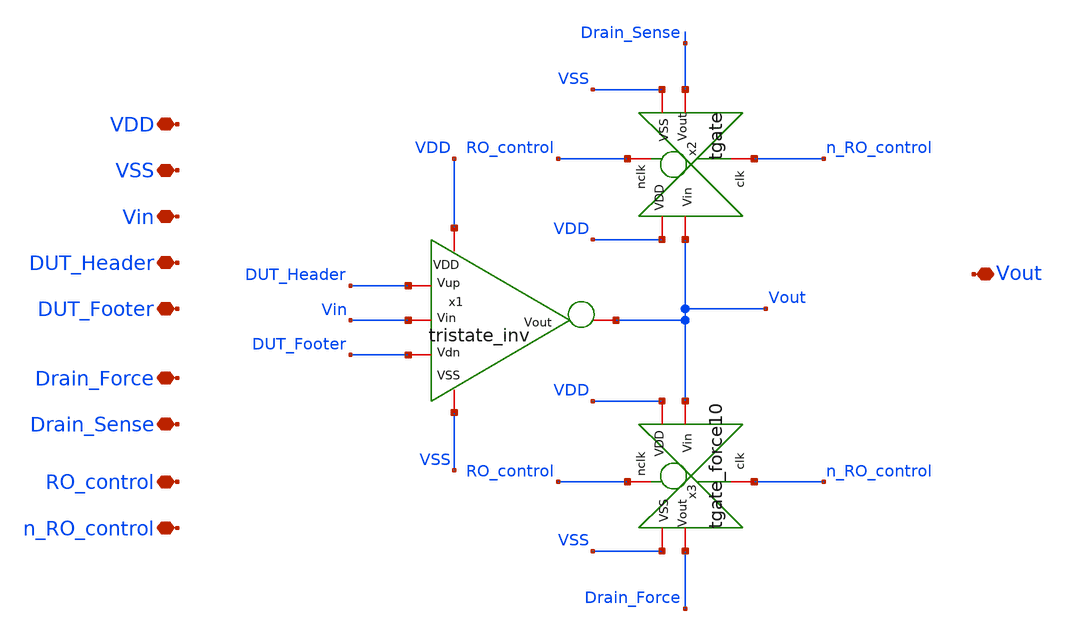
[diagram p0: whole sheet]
** sch_path: TT/rovcel1_10.sch
**.subckt rovcel1_10 VDD VSS Vin DUT_Header DUT_Footer Drain_Force Vout Drain_Sense RO_control
*+ n_RO_control
*.iopin VDD
*.iopin VSS
*.iopin Vin
*.iopin DUT_Header
*.iopin DUT_Footer
*.iopin Drain_Force
*.iopin Vout
*.iopin Drain_Sense
*.iopin RO_control
*.iopin n_RO_control
x1 VDD VSS Vin DUT_Header DUT_Footer Vout tristate_inv
x2 RO_control VDD Vout Drain_Sense VSS n_RO_control tgate
x3 RO_control VDD Vout Drain_Force VSS n_RO_control tgate_force10
**.ends

* expanding   symbol:  /foss/designs/Projects/RO_reliability/xschem/tristate_inv.sym # of pins=6
** sym_path: TT/tristate_inv.sym
** sch_path: TT/tristate_inv.sch
.subckt tristate_inv VDD VSS Vin Vup Vdn Vout
*.iopin VDD
*.iopin VSS
*.iopin Vin
*.iopin Vout
*.iopin Vup
*.iopin Vdn
XM1 net1 Vup VDD VDD sky130_fd_pr__pfet_01v8 L=0.15 W=4.75 nf=1 ad='int((nf+1)/2) * W/nf * 0.29' as='int((nf+2)/2) * W/nf * 0.29'
+ pd='2*int((nf+1)/2) * (W/nf + 0.29)' ps='2*int((nf+2)/2) * (W/nf + 0.29)' nrd='0.29 / W' nrs='0.29 / W'
+ sa=0 sb=0 sd=0 mult=40 m=40
XM2 Vout Vin net1 VDD sky130_fd_pr__pfet_01v8 L=0.15 W=4.75 nf=1 ad='int((nf+1)/2) * W/nf * 0.29' as='int((nf+2)/2) * W/nf * 0.29'
+ pd='2*int((nf+1)/2) * (W/nf + 0.29)' ps='2*int((nf+2)/2) * (W/nf + 0.29)' nrd='0.29 / W' nrs='0.29 / W'
+ sa=0 sb=0 sd=0 mult=4 m=4
XM3 Vout Vin net2 VSS sky130_fd_pr__nfet_01v8 L=0.15 W=2.1 nf=1 ad='int((nf+1)/2) * W/nf * 0.29' as='int((nf+2)/2) * W/nf * 0.29'
+ pd='2*int((nf+1)/2) * (W/nf + 0.29)' ps='2*int((nf+2)/2) * (W/nf + 0.29)' nrd='0.29 / W' nrs='0.29 / W'
+ sa=0 sb=0 sd=0 mult=2 m=2
XM4 net2 Vdn VSS VSS sky130_fd_pr__nfet_01v8 L=0.15 W=2.1 nf=1 ad='int((nf+1)/2) * W/nf * 0.29' as='int((nf+2)/2) * W/nf * 0.29'
+ pd='2*int((nf+1)/2) * (W/nf + 0.29)' ps='2*int((nf+2)/2) * (W/nf + 0.29)' nrd='0.29 / W' nrs='0.29 / W'
+ sa=0 sb=0 sd=0 mult=20 m=20
.ends


* expanding   symbol:  /foss/designs/Projects/RO_reliability/xschem/tgate.sym # of pins=6
** sym_path: TT/tgate.sym
** sch_path: TT/tgate.sch
.subckt tgate nclk VDD Vin Vout VSS clk
*.iopin nclk
*.iopin clk
*.iopin VDD
*.iopin VSS
*.iopin Vout
*.iopin Vin
XM1 Vin nclk Vout VDD sky130_fd_pr__pfet_01v8 L=0.15 W=0.45 nf=1 ad='int((nf+1)/2) * W/nf * 0.29' as='int((nf+2)/2) * W/nf * 0.29'
+ pd='2*int((nf+1)/2) * (W/nf + 0.29)' ps='2*int((nf+2)/2) * (W/nf + 0.29)' nrd='0.29 / W' nrs='0.29 / W'
+ sa=0 sb=0 sd=0 mult=1 m=1
XM2 Vin clk Vout VSS sky130_fd_pr__nfet_01v8 L=0.15 W=0.45 nf=1 ad='int((nf+1)/2) * W/nf * 0.29' as='int((nf+2)/2) * W/nf * 0.29'
+ pd='2*int((nf+1)/2) * (W/nf + 0.29)' ps='2*int((nf+2)/2) * (W/nf + 0.29)' nrd='0.29 / W' nrs='0.29 / W'
+ sa=0 sb=0 sd=0 mult=1 m=1
.ends


* expanding   symbol:  /foss/designs/Projects/RO_reliability/xschem/tgate_force10.sym # of pins=6
** sym_path: TT/tgate_force10.sym
** sch_path: TT/tgate_force10.sch
.subckt tgate_force10 nclk VDD Vin Vout VSS clk
*.iopin nclk
*.iopin clk
*.iopin VDD
*.iopin VSS
*.iopin Vout
*.iopin Vin
XM1 Vin nclk Vout VDD sky130_fd_pr__pfet_01v8 L=0.15 W=4.75 nf=1 ad='int((nf+1)/2) * W/nf * 0.29' as='int((nf+2)/2) * W/nf * 0.29'
+ pd='2*int((nf+1)/2) * (W/nf + 0.29)' ps='2*int((nf+2)/2) * (W/nf + 0.29)' nrd='0.29 / W' nrs='0.29 / W'
+ sa=0 sb=0 sd=0 mult=40 m=40
XM2 Vin clk Vout VSS sky130_fd_pr__nfet_01v8 L=0.15 W=2.1 nf=1 ad='int((nf+1)/2) * W/nf * 0.29' as='int((nf+2)/2) * W/nf * 0.29'
+ pd='2*int((nf+1)/2) * (W/nf + 0.29)' ps='2*int((nf+2)/2) * (W/nf + 0.29)' nrd='0.29 / W' nrs='0.29 / W'
+ sa=0 sb=0 sd=0 mult=20 m=20
.ends

.end
